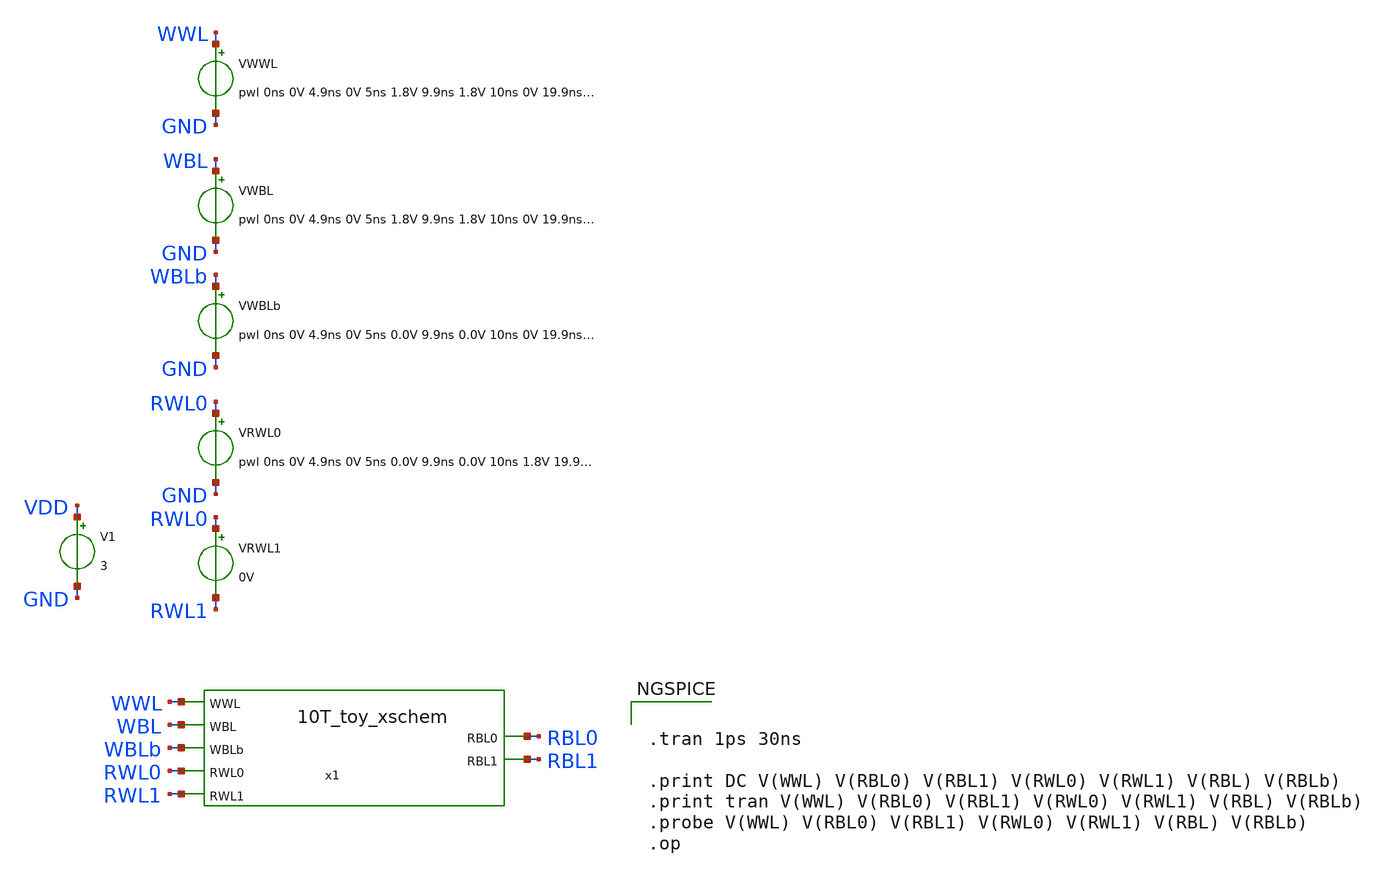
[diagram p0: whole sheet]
** sch_path: custom/xschem/test_10T_toy_xschem.sch
**.subckt test_10T_toy_xschem
V1 VDD GND 3
VWWL WWL GND pwl 0ns 0V 4.9ns 0V 5ns 1.8V 9.9ns 1.8V 10ns 0V 19.9ns 0V 20ns 1.8V 24.9ns 1.8V 25ns 0V
VWBL WBL GND pwl 0ns 0V 4.9ns 0V 5ns 1.8V 9.9ns 1.8V 10ns 0V 19.9ns 0V 20ns 0V 24.9ns 0V 25ns 0V
VRWL1 RWL0 RWL1 0V
VWBLb WBLb GND pwl 0ns 0V 4.9ns 0V 5ns 0.0V 9.9ns 0.0V 10ns 0V 19.9ns 0V 20ns 1.8V 24.9ns 1.8V 25ns
+ 0V
VRWL0 RWL0 GND pwl 0ns 0V 4.9ns 0V 5ns 0.0V 9.9ns 0.0V 10ns 1.8V 19.9ns 1.8V 20ns 0.0V 24.9ns 0.0V
+ 25ns 1.8V
x1 WWL WBL RBL0 RBL1 WBLb RWL0 RWL1 VDD GND 10T_toy_xschem
**** begin user architecture code

.lib $::SKYWATER_MODELS/sky130.lib.spice tt


**** end user architecture code
**.ends

* expanding   symbol:  10T_toy_xschem.sym # of pins=7
** sym_path: custom/xschem/10T_toy_xschem.sym
** sch_path: custom/xschem/10T_toy_xschem.sch
.subckt 10T_toy_xschem WWL WBL RBL0 RBL1 WBLb RWL0 RWL1 VDD GND
*.ipin WWL
*.ipin RWL0
*.ipin RWL1
*.ipin WBL
*.ipin WBLb
*.opin RBL0
*.opin RBL1
x1 net1 net2 VDD GND INVX1
x2 net2 net1 VDD GND INVX1
XM1 net2 WWL WBL GND sky130_fd_pr__nfet_01v8 L=0.15 W=0.14 nf=1 ad='int((nf+1)/2) * W/nf * 0.29' as='int((nf+2)/2) * W/nf * 0.29'
+ pd='2*int((nf+1)/2) * (W/nf + 0.29)' ps='2*int((nf+2)/2) * (W/nf + 0.29)' nrd='0.29 / W' nrs='0.29 / W'
+ sa=0 sb=0 sd=0 mult=1 m=1
XM2 WBLb WWL net1 GND sky130_fd_pr__nfet_01v8 L=0.15 W=0.14 nf=1 ad='int((nf+1)/2) * W/nf * 0.29' as='int((nf+2)/2) * W/nf * 0.29'
+ pd='2*int((nf+1)/2) * (W/nf + 0.29)' ps='2*int((nf+2)/2) * (W/nf + 0.29)' nrd='0.29 / W' nrs='0.29 / W'
+ sa=0 sb=0 sd=0 mult=1 m=1
XM3 net3 net2 GND GND sky130_fd_pr__nfet_01v8 L=0.15 W=0.14 nf=1 ad='int((nf+1)/2) * W/nf * 0.29' as='int((nf+2)/2) * W/nf * 0.29'
+ pd='2*int((nf+1)/2) * (W/nf + 0.29)' ps='2*int((nf+2)/2) * (W/nf + 0.29)' nrd='0.29 / W' nrs='0.29 / W'
+ sa=0 sb=0 sd=0 mult=1 m=1
XM4 RBL0 RWL0 net3 GND sky130_fd_pr__nfet_01v8 L=0.15 W=0.21 nf=1 ad='int((nf+1)/2) * W/nf * 0.29' as='int((nf+2)/2) * W/nf * 0.29'
+ pd='2*int((nf+1)/2) * (W/nf + 0.29)' ps='2*int((nf+2)/2) * (W/nf + 0.29)' nrd='0.29 / W' nrs='0.29 / W'
+ sa=0 sb=0 sd=0 mult=1 m=1
XM5 net4 net1 GND GND sky130_fd_pr__nfet_01v8 L=0.15 W=0.14 nf=1 ad='int((nf+1)/2) * W/nf * 0.29' as='int((nf+2)/2) * W/nf * 0.29'
+ pd='2*int((nf+1)/2) * (W/nf + 0.29)' ps='2*int((nf+2)/2) * (W/nf + 0.29)' nrd='0.29 / W' nrs='0.29 / W'
+ sa=0 sb=0 sd=0 mult=1 m=1
XM6 RBL1 RWL1 net4 GND sky130_fd_pr__nfet_01v8 L=0.15 W=0.21 nf=1 ad='int((nf+1)/2) * W/nf * 0.29' as='int((nf+2)/2) * W/nf * 0.29'
+ pd='2*int((nf+1)/2) * (W/nf + 0.29)' ps='2*int((nf+2)/2) * (W/nf + 0.29)' nrd='0.29 / W' nrs='0.29 / W'
+ sa=0 sb=0 sd=0 mult=1 m=1
.ends


* expanding   symbol:  INVX1.sym # of pins=2
** sym_path: custom/xschem/INVX1.sym
** sch_path: custom/xschem/INVX1.sch
.subckt INVX1 Y A VDD GND
*.ipin A
*.opin Y
XM1 Y A GND GND sky130_fd_pr__nfet_01v8 L=0.15 W=0.21 nf=1 ad='int((nf+1)/2) * W/nf * 0.29' as='int((nf+2)/2) * W/nf * 0.29'
+ pd='2*int((nf+1)/2) * (W/nf + 0.29)' ps='2*int((nf+2)/2) * (W/nf + 0.29)' nrd='0.29 / W' nrs='0.29 / W'
+ sa=0 sb=0 sd=0 mult=1 m=1
XM2 Y A VDD VDD sky130_fd_pr__pfet_01v8 L=0.15 W=0.14 nf=1 ad='int((nf+1)/2) * W/nf * 0.29' as='int((nf+2)/2) * W/nf * 0.29'
+ pd='2*int((nf+1)/2) * (W/nf + 0.29)' ps='2*int((nf+2)/2) * (W/nf + 0.29)' nrd='0.29 / W' nrs='0.29 / W'
+ sa=0 sb=0 sd=0 mult=1 m=1
.ends

**** begin user architecture code


.tran 1ps 30ns

.print DC V(WWL) V(RBL0) V(RBL1) V(RWL0) V(RWL1) V(RBL) V(RBLb)
.print tran V(WWL) V(RBL0) V(RBL1) V(RWL0) V(RWL1) V(RBL) V(RBLb)
.probe V(WWL) V(RBL0) V(RBL1) V(RWL0) V(RWL1) V(RBL) V(RBLb)
.op


**** end user architecture code
.end
